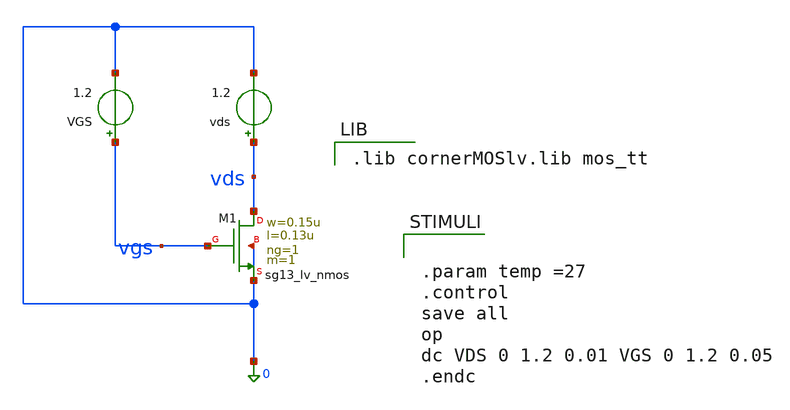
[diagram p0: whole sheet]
** sch_path: nmos_tb.sch
**.subckt nmos_tb
XM1 vds vgs 0 0 sg13_lv_nmos w=0.15u l=0.13u ng=1 m=1 mm_ok=1
vds vds 0 1.2
VGS vgs 0 1.2
**** begin user architecture code

.lib cornerMOSlv.lib mos_tt



.param temp =27
.control
save all
op
dc VDS 0 1.2 0.01 VGS 0 1.2 0.05
.endc


**** end user architecture code
**.ends
.end
